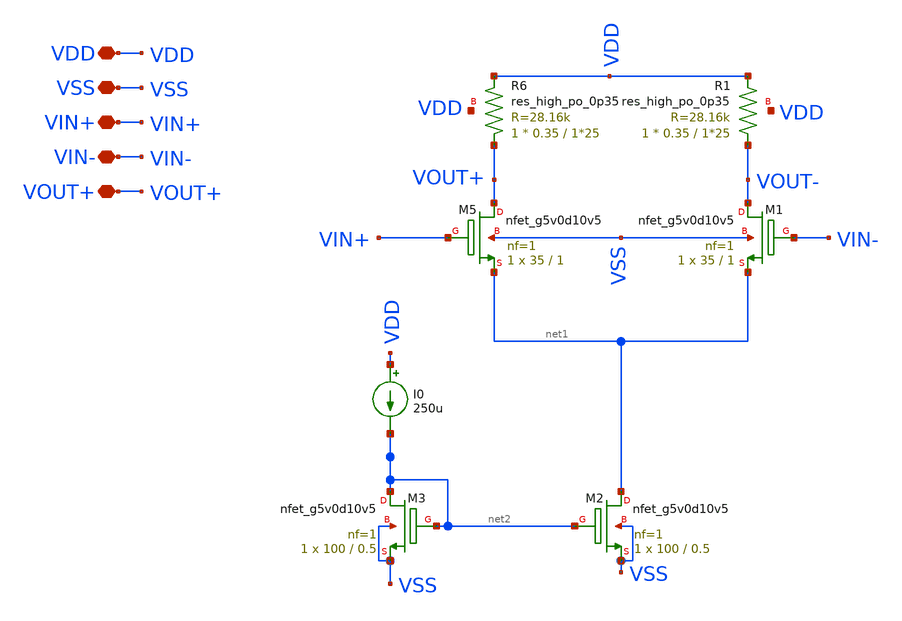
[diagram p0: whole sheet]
** sch_path: old stuff/amplifiers/differencial_stage_amps/basic_stages/basic_NMOS_resistive_stage/differential_stage.sch
**.subckt differential_stage VDD VSS VIN+ VIN- VOUT+
*.iopin VDD
*.iopin VSS
*.iopin VIN+
*.iopin VIN-
*.iopin VOUT+
XM5 VOUT+ VIN+ net1 VSS sky130_fd_pr__nfet_g5v0d10v5 L=1 W=35 nf=1 ad='int((1 + 1)/2) * 35 / 1 * 0.29'
+ as='int((1 + 2)/2) * 35 / 1 * 0.29' pd='2*int((1 + 1)/2) * (35 / 1 + 0.29)' ps='2*int((1 + 2)/2) * (35 / 1 + 0.29)'
+ nrd='0.29 / 35 ' nrs='0.29 / 35 ' sa=0 sb=0 sd=0 mult=1 m=1
XM1 VOUT- VIN- net1 VSS sky130_fd_pr__nfet_g5v0d10v5 L=1 W=35 nf=1 ad='int((1 + 1)/2) * 35 / 1 * 0.29'
+ as='int((1 + 2)/2) * 35 / 1 * 0.29' pd='2*int((1 + 1)/2) * (35 / 1 + 0.29)' ps='2*int((1 + 2)/2) * (35 / 1 + 0.29)'
+ nrd='0.29 / 35 ' nrs='0.29 / 35 ' sa=0 sb=0 sd=0 mult=1 m=1
XR6 VOUT+ VDD VDD sky130_fd_pr__res_high_po_0p35 L=1*25 mult=1 m=1
XR1 VOUT- VDD VDD sky130_fd_pr__res_high_po_0p35 L=1*25 mult=1 m=1
XM2 net1 net2 VSS VSS sky130_fd_pr__nfet_g5v0d10v5 L=0.5 W=100 nf=1 ad='int((1 + 1)/2) * 100 / 1 * 0.29'
+ as='int((1 + 2)/2) * 100 / 1 * 0.29' pd='2*int((1 + 1)/2) * (100 / 1 + 0.29)' ps='2*int((1 + 2)/2) * (100 / 1 + 0.29)'
+ nrd='0.29 / 100 ' nrs='0.29 / 100 ' sa=0 sb=0 sd=0 mult=1 m=1
XM3 net2 net2 VSS VSS sky130_fd_pr__nfet_g5v0d10v5 L=0.5 W=100 nf=1 ad='int((1 + 1)/2) * 100 / 1 * 0.29'
+ as='int((1 + 2)/2) * 100 / 1 * 0.29' pd='2*int((1 + 1)/2) * (100 / 1 + 0.29)' ps='2*int((1 + 2)/2) * (100 / 1 + 0.29)'
+ nrd='0.29 / 100 ' nrs='0.29 / 100 ' sa=0 sb=0 sd=0 mult=1 m=1
I0 VDD net2 250u
**.ends
.end
